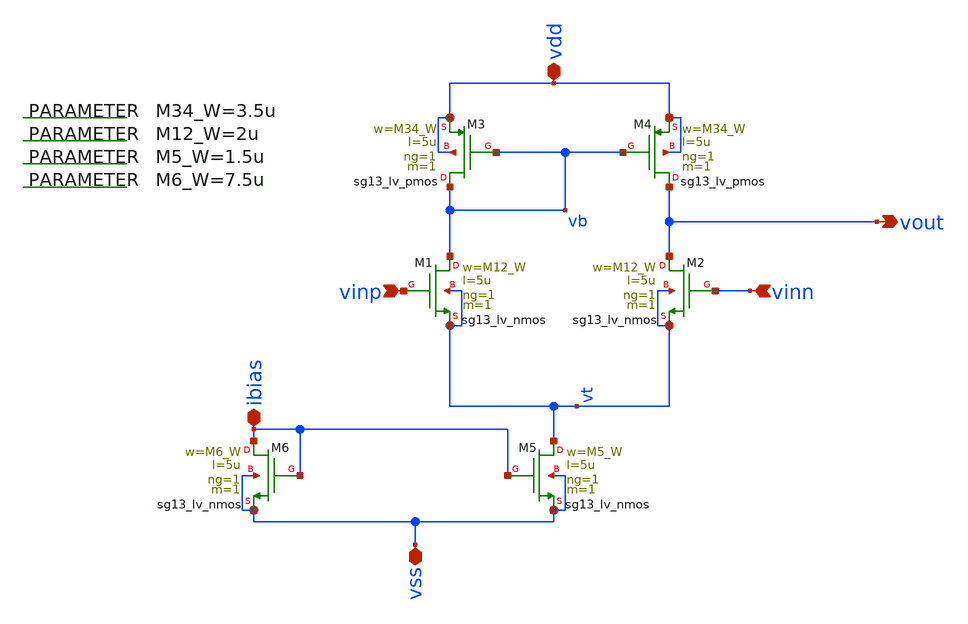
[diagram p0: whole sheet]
** sch_path: 004_Real_Circuits/5T-OTA.sch
**.subckt 5T-OTA vinp vdd vss vout vinn ibias
*.ipin vinp
*.iopin vdd
*.iopin vss
*.opin vout
*.ipin vinn
*.iopin ibias
XM1 vb vinp vt vt sg13_lv_nmos w=M12_W l=5u ng=1 m=1 mm_ok=1
XM5 vt ibias vss vss sg13_lv_nmos w=M5_W l=5u ng=1 m=1 mm_ok=1
XM2 vout vinn vt vt sg13_lv_nmos w=M12_W l=5u ng=1 m=1 mm_ok=1
XM6 ibias ibias vss vss sg13_lv_nmos w=M6_W l=5u ng=1 m=1 mm_ok=1
XM3 vb vb vdd vdd sg13_lv_pmos w=M34_W l=5u ng=1 m=1 mm_ok=1
XM4 vout vb vdd vdd sg13_lv_pmos w=M34_W l=5u ng=1 m=1 mm_ok=1
.param M34_W=3.5u
.param M12_W=2u
.param M5_W=1.5u
.param M6_W=7.5u
**.ends
.end
